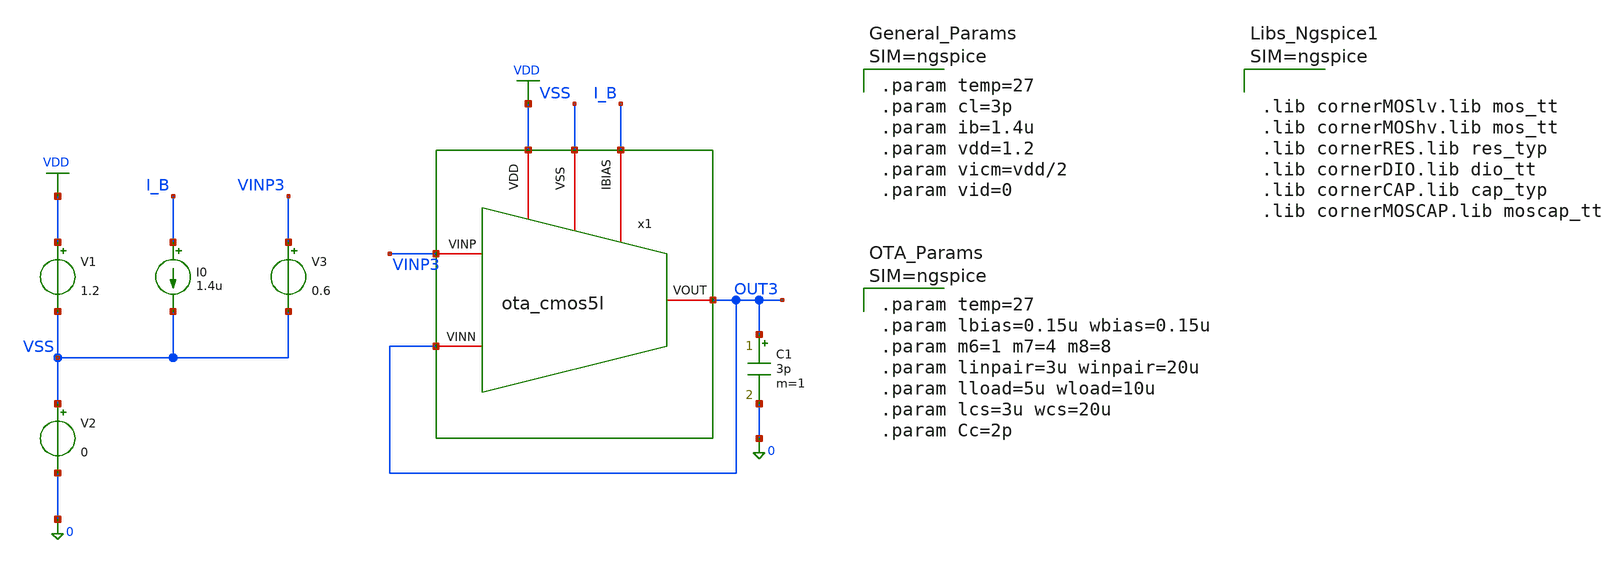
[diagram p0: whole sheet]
** sch_path: xschem/ota_cmos5l/tb/tb_ota_cmos5l_TRAN_large/tb_ota_cmos5l_TRAN_large.sch
**.subckt tb_ota_cmos5l_TRAN_large
x1 VSS I_B VDD OUT3 VINP3 OUT3 ota_cmos5l
C1 OUT3 0 3p m=1
I0 I_B VSS 1.4u
V1 VDD VSS 1.2
V2 VSS 0 0
V3 VINP3 VSS 0.6
**** begin user architecture code



.lib cornerMOSlv.lib mos_tt
.lib cornerMOShv.lib mos_tt
.lib cornerRES.lib res_typ
.lib cornerDIO.lib dio_tt
.lib cornerCAP.lib cap_typ
.lib cornerMOSCAP.lib moscap_tt





.param temp=27
.param cl=3p
.param ib=1.4u
.param vdd=1.2
.param vicm=vdd/2
.param vid=0





.param temp=27
.param lbias=0.15u wbias=0.15u
.param m6=1 m7=4 m8=8
.param linpair=3u winpair=20u
.param lload=5u wload=10u
.param lcs=3u wcs=20u
.param Cc=2p





.control
shell mkdir -p result

* LARGE-SIGNAL STEP RESPONSE (SLEW RATE & PROPAGATION DELAYS)
* Stimulus: Pulse swing 0.2 V to 1.0 V (Delta V = 0.8 V, Vcm = 0.6 V)
alter @v3[pulse] = [ 0.2 1.0 20n 1n 1n 2u 5u ]

tran 0.2n 5u
run

let v_inl  = v(vinp3)
let v_outl = v(out3)

* --- Rising Edge Analysis ---
* Input 50% crossing (0.60 V)
meas tran t_in_r50  when v_inl=0.60 rise=1

* Output 10% (0.28 V), 50% (0.60 V), and 90% (0.92 V) crossings
meas tran t_out_r10 when v_outl=0.28 rise=1
meas tran t_out_r50 when v_outl=0.60 rise=1
meas tran t_out_r90 when v_outl=0.92 rise=1

* Compute Rise Time, Positive Slew Rate (SR+), and Propagation Delay (tpLH)
let t_rise_ns = (t_out_r90 - t_out_r10) * 1e9
let sr_pos    = (0.92 - 0.28) / (t_out_r90 - t_out_r10) / 1e6
let t_plh_ns  = (t_out_r50 - t_in_r50) * 1e9

* --- Falling Edge Analysis ---
* Input 50% crossing (0.60 V)
meas tran t_in_f50  when v_inl=0.60 fall=1

* Output 90% (0.92 V), 50% (0.60 V), and 10% (0.28 V) crossings
meas tran t_out_f90 when v_outl=0.92 fall=1
meas tran t_out_f50 when v_outl=0.60 fall=1
meas tran t_out_f10 when v_outl=0.28 fall=1

* Compute Fall Time, Negative Slew Rate (SR-), and Propagation Delay (tpHL)
let t_fall_ns = (t_out_f10 - t_out_f90) * 1e9
let sr_neg    = (0.92 - 0.28) / (t_out_f10 - t_out_f90) / 1e6
let t_phl_ns  = (t_out_f50 - t_in_f50) * 1e9

* Save output waveforms to the specified rawfile
write ./result/tb_cg_ota_tran_large.raw v_inl v_outl

* Print execution summary
echo "======================================================="
echo "   OTA LARGE-SIGNAL TRANSIENT SIMULATION RESULTS       "
echo "======================================================="
echo " Positive Slew Rate (SR+)  : " $&sr_pos    " V/us"
echo " Negative Slew Rate (SR-)  : " $&sr_neg    " V/us"
echo " Rise Time 10% - 90% (tr)  : " $&t_rise_ns " ns"
echo " Fall Time 90% - 10% (tf)  : " $&t_fall_ns " ns"
echo " Propagation Delay (tpLH)  : " $&t_plh_ns  " ns"
echo " Propagation Delay (tpHL)  : " $&t_phl_ns  " ns"
echo "======================================================="

* Reset v5 source back to clean DC operating point
alter @v5[pulse] = [ 0.6 0.6 0 0 0 1u 2u ]

plot v_outl v_inl
.endc


**** end user architecture code
**.ends

* expanding   symbol:  /foss/designs/sg13cmos5l_spma_ip__instramp/xschem/ota_cmos5l/ota_cmos5l.sym #
*+ of pins=6
** sym_path: xschem/output_buffer/ota_cmos5l.sym
** sch_path: xschem/output_buffer/ota_cmos5l.sch
.subckt ota_cmos5l VSS IBIAS VDD VINN VINP VOUT
*.iopin IBIAS
*.iopin VDD
*.iopin VSS
*.iopin VOUT
*.iopin VINP
*.iopin VINN
XM6 IBIAS IBIAS VDD VDD sg13_lv_pmos w={wbias} l={lbias} ng=1 m={m6} mm_ok=1
XM7 net1 IBIAS VDD VDD sg13_lv_pmos w={wbias} l={lbias} ng=1 m={m7} mm_ok=1
XM8 VOUT IBIAS VDD VDD sg13_lv_pmos w={wbias} l={lbias} ng=1 m={m8} mm_ok=1
XM1 net2 VINN net1 VDD sg13_lv_pmos w={winpair} l={linpair} ng=1 m=1 mm_ok=1
XM2 net3 VINP net1 VDD sg13_lv_pmos w={winpair} l={linpair} ng=1 m=1 mm_ok=1
XM3 net2 net2 VSS VSS sg13_lv_nmos w={wload} l={lload} ng=1 m=1 mm_ok=1
XM4 net3 net2 VSS VSS sg13_lv_nmos w={wload} l={lload} ng=1 m=1 mm_ok=1
XM5 VOUT net3 VSS VSS sg13_lv_nmos w={wcs} l={lcs} ng=1 m=1 mm_ok=1
XR1 net3 net4 VSS rhigh w=0.5e-6 l=1.95e-6 m=1 b=0 mm_ok=1
.save v(vinp)
.save v(vinn)
.save v(vout)
XC2 VOUT net4 cap_cmomi w=15e-6 l=15e-6 mmin=1 mmax=4 feed=double subblock=0 m=5 mm_ok=1
**** begin user architecture code


.param temp=27
.param lbias=0.15u wbias=0.15u
.param m6=1 m7=4 m8=8
.param linpair=3u winpair=20u
.param lload=5u wload=10u
.param lcs=3u wcs=20u
.param Cc=2p



**** end user architecture code
XC1 VOUT net4 cap_cmomi w=15e-6 l=15e-6 mmin=1 mmax=4 feed=double subblock=0 m=4 mm_ok=1
.ends

.GLOBAL VDD
.end
